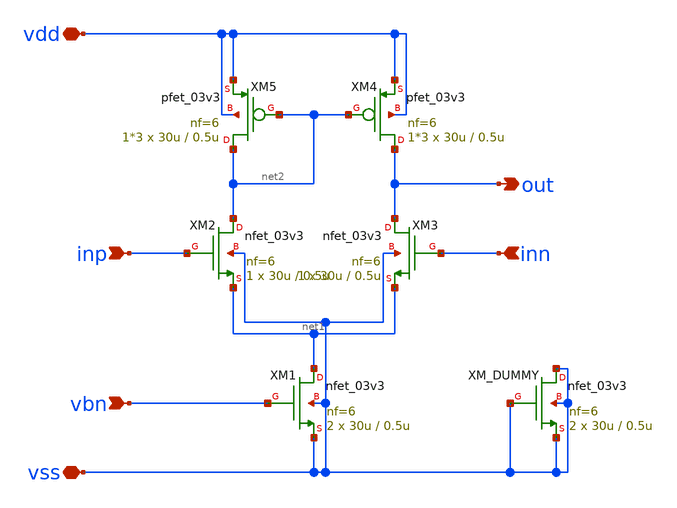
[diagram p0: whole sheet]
** sch_path: designs/libs/example/ota_nmos/ota_nmos.sch
**.subckt ota_nmos inp inn out vbn vss vdd
*.ipin inp
*.ipin inn
*.opin out
*.ipin vbn
*.iopin vss
*.iopin vdd
XM1 net1 vbn vss vss nfet_03v3 L=0.5u W=30u nf=6 ad='int((nf+1)/2) * W/nf * 0.18u' as='int((nf+2)/2) * W/nf * 0.18u'
+ pd='2*int((nf+1)/2) * (W/nf + 0.18u)' ps='2*int((nf+2)/2) * (W/nf + 0.18u)' nrd='0.18u / W' nrs='0.18u / W'
+ sa=0 sb=0 sd=0 m=2
XM2 net2 inp net1 vss nfet_03v3 L=0.5u W=30u nf=6 ad='int((nf+1)/2) * W/nf * 0.18u' as='int((nf+2)/2) * W/nf * 0.18u'
+ pd='2*int((nf+1)/2) * (W/nf + 0.18u)' ps='2*int((nf+2)/2) * (W/nf + 0.18u)' nrd='0.18u / W' nrs='0.18u / W'
+ sa=0 sb=0 sd=0 m=1
XM3 out inn net1 vss nfet_03v3 L=0.5u W=30u nf=6 ad='int((nf+1)/2) * W/nf * 0.18u' as='int((nf+2)/2) * W/nf * 0.18u'
+ pd='2*int((nf+1)/2) * (W/nf + 0.18u)' ps='2*int((nf+2)/2) * (W/nf + 0.18u)' nrd='0.18u / W' nrs='0.18u / W'
+ sa=0 sb=0 sd=0 m=1
XM4 out net2 vdd vdd pfet_03v3 L=0.5u W=30u nf=6 ad='int((nf+1)/2) * W/nf * 0.18u' as='int((nf+2)/2) * W/nf * 0.18u'
+ pd='2*int((nf+1)/2) * (W/nf + 0.18u)' ps='2*int((nf+2)/2) * (W/nf + 0.18u)' nrd='0.18u / W' nrs='0.18u / W'
+ sa=0 sb=0 sd=0 m=1*3
XM5 net2 net2 vdd vdd pfet_03v3 L=0.5u W=30u nf=6 ad='int((nf+1)/2) * W/nf * 0.18u' as='int((nf+2)/2) * W/nf * 0.18u'
+ pd='2*int((nf+1)/2) * (W/nf + 0.18u)' ps='2*int((nf+2)/2) * (W/nf + 0.18u)' nrd='0.18u / W' nrs='0.18u / W'
+ sa=0 sb=0 sd=0 m=1*3
XM_DUMMY vss vss vss vss nfet_03v3 L=0.5u W=30u nf=6 ad='int((nf+1)/2) * W/nf * 0.18u' as='int((nf+2)/2) * W/nf * 0.18u'
+ pd='2*int((nf+1)/2) * (W/nf + 0.18u)' ps='2*int((nf+2)/2) * (W/nf + 0.18u)' nrd='0.18u / W' nrs='0.18u / W'
+ sa=0 sb=0 sd=0 m=2
**.ends
.end
